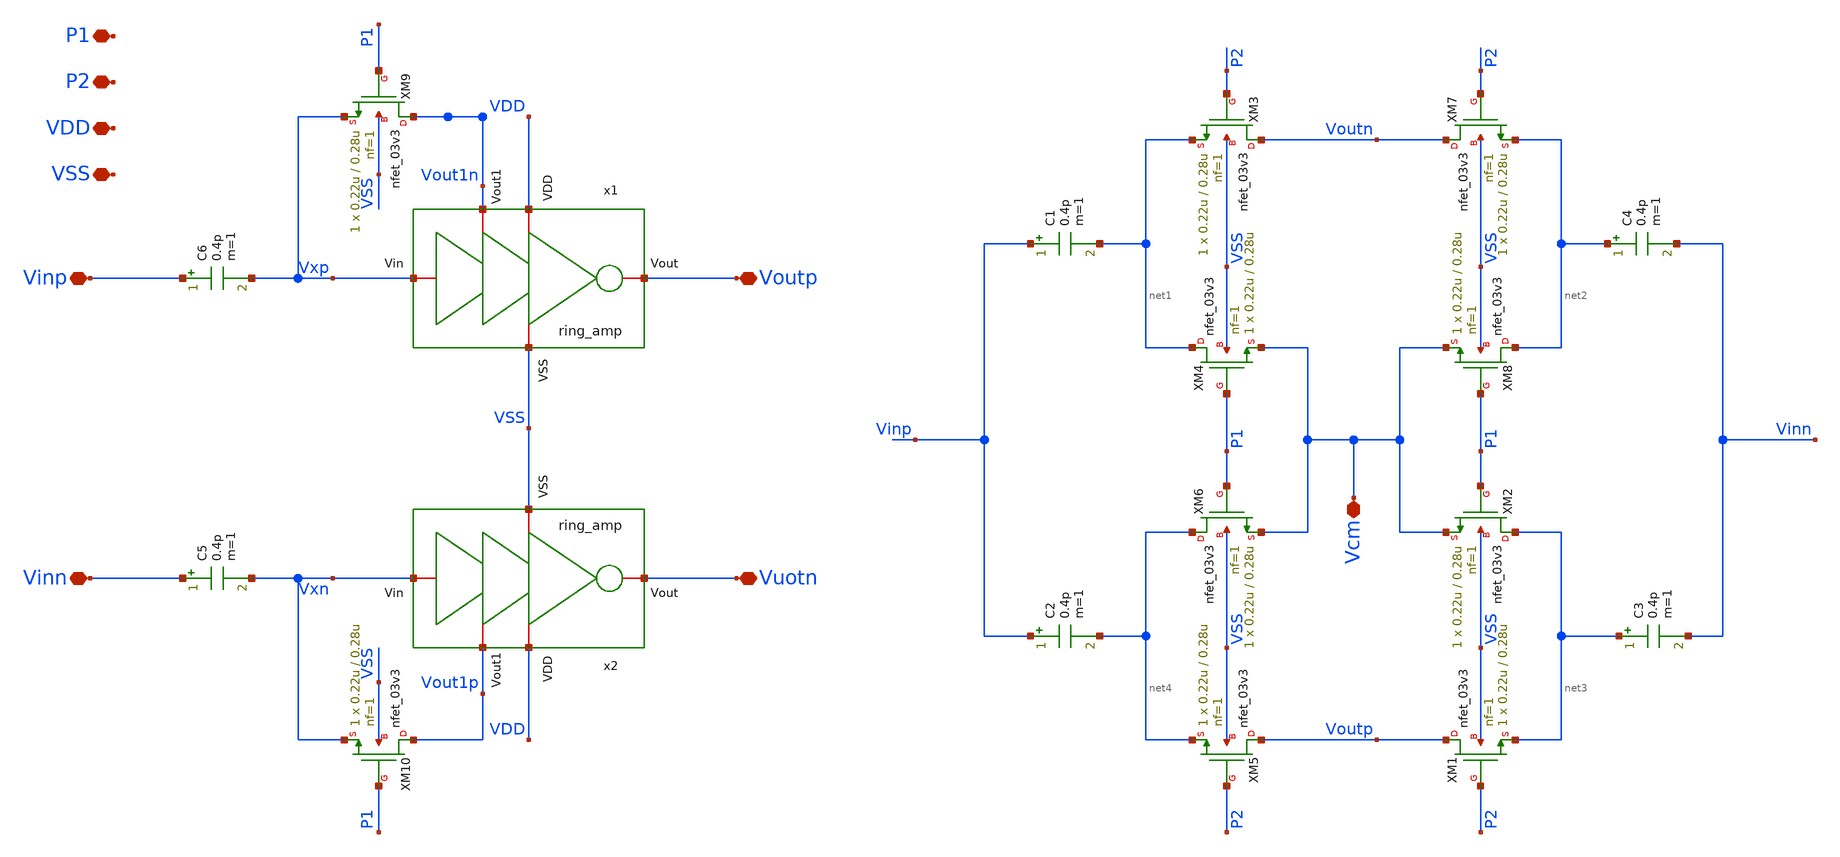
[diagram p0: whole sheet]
** sch_path: designs/DS_modulator/ring_amp_diff/xschem/ring_amp_diff.sch
**.subckt ring_amp_diff P1 P2 VDD VSS Vcm Vinp Vinn Voutp Vuotn
*.iopin P1
*.iopin P2
*.iopin VDD
*.iopin VSS
*.iopin Vcm
*.iopin Vinp
*.iopin Vinn
*.iopin Voutp
*.iopin Vuotn
XM1 Voutp P2 net3 VSS nfet_03v3 L=0.28u W=0.22u nf=1 ad='int((nf+1)/2) * W/nf * 0.18u' as='int((nf+2)/2) * W/nf * 0.18u'
+ pd='2*int((nf+1)/2) * (W/nf + 0.18u)' ps='2*int((nf+2)/2) * (W/nf + 0.18u)' nrd='0.18u / W' nrs='0.18u / W'
+ sa=0 sb=0 sd=0 m=1
XM2 net3 P1 Vcm VSS nfet_03v3 L=0.28u W=0.22u nf=1 ad='int((nf+1)/2) * W/nf * 0.18u' as='int((nf+2)/2) * W/nf * 0.18u'
+ pd='2*int((nf+1)/2) * (W/nf + 0.18u)' ps='2*int((nf+2)/2) * (W/nf + 0.18u)' nrd='0.18u / W' nrs='0.18u / W'
+ sa=0 sb=0 sd=0 m=1
XM3 Voutn P2 net1 VSS nfet_03v3 L=0.28u W=0.22u nf=1 ad='int((nf+1)/2) * W/nf * 0.18u' as='int((nf+2)/2) * W/nf * 0.18u'
+ pd='2*int((nf+1)/2) * (W/nf + 0.18u)' ps='2*int((nf+2)/2) * (W/nf + 0.18u)' nrd='0.18u / W' nrs='0.18u / W'
+ sa=0 sb=0 sd=0 m=1
XM4 net1 P1 Vcm VSS nfet_03v3 L=0.28u W=0.22u nf=1 ad='int((nf+1)/2) * W/nf * 0.18u' as='int((nf+2)/2) * W/nf * 0.18u'
+ pd='2*int((nf+1)/2) * (W/nf + 0.18u)' ps='2*int((nf+2)/2) * (W/nf + 0.18u)' nrd='0.18u / W' nrs='0.18u / W'
+ sa=0 sb=0 sd=0 m=1
XM5 Voutp P2 net4 VSS nfet_03v3 L=0.28u W=0.22u nf=1 ad='int((nf+1)/2) * W/nf * 0.18u' as='int((nf+2)/2) * W/nf * 0.18u'
+ pd='2*int((nf+1)/2) * (W/nf + 0.18u)' ps='2*int((nf+2)/2) * (W/nf + 0.18u)' nrd='0.18u / W' nrs='0.18u / W'
+ sa=0 sb=0 sd=0 m=1
XM6 net4 P1 Vcm VSS nfet_03v3 L=0.28u W=0.22u nf=1 ad='int((nf+1)/2) * W/nf * 0.18u' as='int((nf+2)/2) * W/nf * 0.18u'
+ pd='2*int((nf+1)/2) * (W/nf + 0.18u)' ps='2*int((nf+2)/2) * (W/nf + 0.18u)' nrd='0.18u / W' nrs='0.18u / W'
+ sa=0 sb=0 sd=0 m=1
XM7 Voutn P2 net2 VSS nfet_03v3 L=0.28u W=0.22u nf=1 ad='int((nf+1)/2) * W/nf * 0.18u' as='int((nf+2)/2) * W/nf * 0.18u'
+ pd='2*int((nf+1)/2) * (W/nf + 0.18u)' ps='2*int((nf+2)/2) * (W/nf + 0.18u)' nrd='0.18u / W' nrs='0.18u / W'
+ sa=0 sb=0 sd=0 m=1
XM8 net2 P1 Vcm VSS nfet_03v3 L=0.28u W=0.22u nf=1 ad='int((nf+1)/2) * W/nf * 0.18u' as='int((nf+2)/2) * W/nf * 0.18u'
+ pd='2*int((nf+1)/2) * (W/nf + 0.18u)' ps='2*int((nf+2)/2) * (W/nf + 0.18u)' nrd='0.18u / W' nrs='0.18u / W'
+ sa=0 sb=0 sd=0 m=1
XM9 Vout1n P1 Vxp VSS nfet_03v3 L=0.28u W=0.22u nf=1 ad='int((nf+1)/2) * W/nf * 0.18u' as='int((nf+2)/2) * W/nf * 0.18u'
+ pd='2*int((nf+1)/2) * (W/nf + 0.18u)' ps='2*int((nf+2)/2) * (W/nf + 0.18u)' nrd='0.18u / W' nrs='0.18u / W'
+ sa=0 sb=0 sd=0 m=1
XM10 Vout1p P1 Vxn VSS nfet_03v3 L=0.28u W=0.22u nf=1 ad='int((nf+1)/2) * W/nf * 0.18u' as='int((nf+2)/2) * W/nf * 0.18u'
+ pd='2*int((nf+1)/2) * (W/nf + 0.18u)' ps='2*int((nf+2)/2) * (W/nf + 0.18u)' nrd='0.18u / W' nrs='0.18u / W'
+ sa=0 sb=0 sd=0 m=1
C1 Vinp net1 0.4p m=1
C2 Vinp net4 0.4p m=1
C3 net3 Vinn 0.4p m=1
C4 net2 Vinn 0.4p m=1
C5 Vinn Vxn 0.4p m=1
C6 Vinp Vxp 0.4p m=1
x1 VDD Vxp Voutp Vout1n VSS ring_amp
x2 VDD Vxn Vuotn Vout1p VSS ring_amp
**.ends
.end
